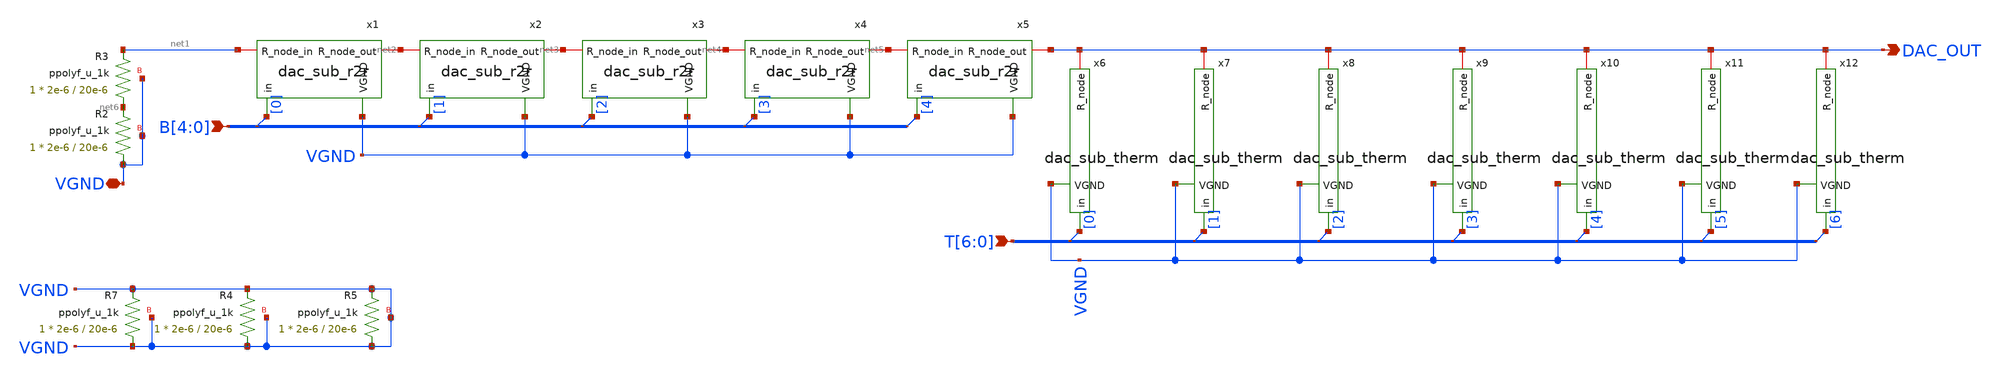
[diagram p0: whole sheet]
** sch_path: xschem/dac_5_3.sch
**.subckt dac_5_3 B[4],B[3],B[2],B[1],B[0] T[6],T[5],T[4],T[3],T[2],T[1],T[0] DAC_OUT VGND
*.ipin B[4],B[3],B[2],B[1],B[0]
*.ipin T[6],T[5],T[4],T[3],T[2],T[1],T[0]
*.opin DAC_OUT
*.iopin VGND
x1 net2 net1 B[0] VGND dac_sub_r2r
x2 net3 net2 B[1] VGND dac_sub_r2r
x3 net4 net3 B[2] VGND dac_sub_r2r
x4 net5 net4 B[3] VGND dac_sub_r2r
x5 DAC_OUT net5 B[4] VGND dac_sub_r2r
* tap: B[4:0] --> B[0]
* tap: B[4:0] --> B[1]
* tap: B[4:0] --> B[2]
* tap: B[4:0] --> B[3]
* tap: B[4:0] --> B[4]
x6 DAC_OUT T[0] VGND dac_sub_therm
x7 DAC_OUT T[1] VGND dac_sub_therm
x8 DAC_OUT T[2] VGND dac_sub_therm
x9 DAC_OUT T[3] VGND dac_sub_therm
x10 DAC_OUT T[4] VGND dac_sub_therm
x11 DAC_OUT T[5] VGND dac_sub_therm
x12 DAC_OUT T[6] VGND dac_sub_therm
* tap: T[6:0] --> T[0]
* tap: T[6:0] --> T[1]
* tap: T[6:0] --> T[2]
* tap: T[6:0] --> T[3]
* tap: T[6:0] --> T[4]
* tap: T[6:0] --> T[5]
* tap: T[6:0] --> T[6]
XR2 VGND net6 VGND ppolyf_u_1k r_width=2e-6 r_length=20e-6 m=1
XR3 net6 net1 VGND ppolyf_u_1k r_width=2e-6 r_length=20e-6 m=1
XR4 VGND VGND VGND ppolyf_u_1k r_width=2e-6 r_length=20e-6 m=1
XR5 VGND VGND VGND ppolyf_u_1k r_width=2e-6 r_length=20e-6 m=1
XR7 VGND VGND VGND ppolyf_u_1k r_width=2e-6 r_length=20e-6 m=1
**.ends

* expanding   symbol:  dac_sub_r2r.sym # of pins=4
** sym_path: xschem/dac_sub_r2r.sym
** sch_path: xschem/dac_sub_r2r.sch
.subckt dac_sub_r2r R_node_out R_node_in in VGND
*.ipin in
*.iopin R_node_out
*.iopin R_node_in
*.iopin VGND
XR7 in net1 VGND ppolyf_u_1k r_width=2e-6 r_length=20e-6 m=1
XR1 net1 R_node_in VGND ppolyf_u_1k r_width=2e-6 r_length=20e-6 m=1
XR2 net2 R_node_in VGND ppolyf_u_1k r_width=2e-6 r_length=20e-6 m=1
XR3 R_node_out net2 VGND ppolyf_u_1k r_width=2e-6 r_length=20e-6 m=1
XR4 net3 R_node_in VGND ppolyf_u_1k r_width=2e-6 r_length=20e-6 m=1
XR5 R_node_out net3 VGND ppolyf_u_1k r_width=2e-6 r_length=20e-6 m=1
.ends


* expanding   symbol:  dac_sub_therm.sym # of pins=3
** sym_path: xschem/dac_sub_therm.sym
** sch_path: xschem/dac_sub_therm.sch
.subckt dac_sub_therm R_node in VGND
*.ipin in
*.iopin R_node
*.iopin VGND
XR7 in net1 VGND ppolyf_u_1k r_width=2e-6 r_length=20e-6 m=1
XR1 net1 R_node VGND ppolyf_u_1k r_width=2e-6 r_length=20e-6 m=1
.ends

.end
